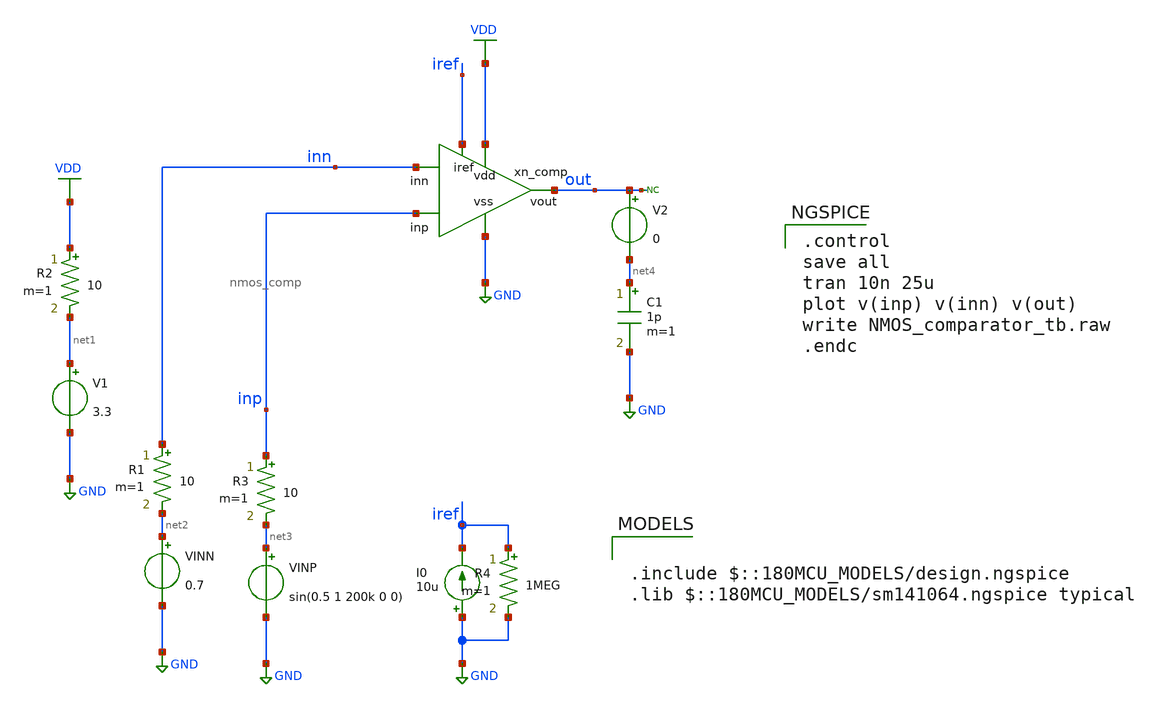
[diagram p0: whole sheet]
** sch_path: designs/libs/tb_analog/tb_nmos_comp/tb_nmos_comp.sch
**.subckt tb_nmos_comp
I0 GND iref 10u
V1 net1 GND 3.3
VINP net3 GND sin(0.5 1 200k 0 0)
* noconn out
VINN net2 GND 0.7
C1 net4 GND 1p m=1
R3 inp net3 10 m=1
R1 inn net2 10 m=1
R2 VDD net1 10 m=1
R4 iref GND 1MEG m=1
V2 out net4 0
xn_comp VDD out inp GND inn iref nmos_comp
**** begin user architecture code

.control
save all
tran 10n 25u
plot v(inp) v(inn) v(out)
write NMOS_comparator_tb.raw
.endc



.include $::180MCU_MODELS/design.ngspice
.lib $::180MCU_MODELS/sm141064.ngspice typical

**** end user architecture code
**.ends

* expanding   symbol:  pmos_comp/nmos_comp.sym # of pins=6
** sym_path: designs/libs/core_analog/nmos_comp/nmos_comp.sym
** sch_path: designs/libs/core_analog/nmos_comp/nmos_comp.sch
.subckt nmos_comp vdd vout inp vss inn iref
*.ipin vss
*.ipin vdd
*.ipin iref
*.ipin inn
*.ipin inp
*.opin vout
XM3 net1 net1 vss vss nfet_03v3 L=1u W=3.5u nf=1 ad='int((nf+1)/2) * W/nf * 0.18u' as='int((nf+2)/2) * W/nf * 0.18u'
+ pd='2*int((nf+1)/2) * (W/nf + 0.18u)' ps='2*int((nf+2)/2) * (W/nf + 0.18u)' nrd='0.18u / W' nrs='0.18u / W'
+ sa=0 sb=0 sd=0 m=1
XM4 vout net1 vss vss nfet_03v3 L=1u W=3.5u nf=1 ad='int((nf+1)/2) * W/nf * 0.18u' as='int((nf+2)/2) * W/nf * 0.18u'
+ pd='2*int((nf+1)/2) * (W/nf + 0.18u)' ps='2*int((nf+2)/2) * (W/nf + 0.18u)' nrd='0.18u / W' nrs='0.18u / W'
+ sa=0 sb=0 sd=0 m=1
XM1 net2 inn i_bias_n vss nfet_03v3 L=1u W=4u nf=1 ad='int((nf+1)/2) * W/nf * 0.18u' as='int((nf+2)/2) * W/nf * 0.18u'
+ pd='2*int((nf+1)/2) * (W/nf + 0.18u)' ps='2*int((nf+2)/2) * (W/nf + 0.18u)' nrd='0.18u / W' nrs='0.18u / W'
+ sa=0 sb=0 sd=0 m=1
XM2 net3 inp i_bias_n vss nfet_03v3 L=1u W=4u nf=1 ad='int((nf+1)/2) * W/nf * 0.18u' as='int((nf+2)/2) * W/nf * 0.18u'
+ pd='2*int((nf+1)/2) * (W/nf + 0.18u)' ps='2*int((nf+2)/2) * (W/nf + 0.18u)' nrd='0.18u / W' nrs='0.18u / W'
+ sa=0 sb=0 sd=0 m=1
XM10 net1 net2 vdd vdd pfet_03v3 L=0.5u W=16.5u nf=4 ad='int((nf+1)/2) * W/nf * 0.18u' as='int((nf+2)/2) * W/nf * 0.18u'
+ pd='2*int((nf+1)/2) * (W/nf + 0.18u)' ps='2*int((nf+2)/2) * (W/nf + 0.18u)' nrd='0.18u / W' nrs='0.18u / W'
+ sa=0 sb=0 sd=0 m=1
XM6 net3 net3 vdd vdd pfet_03v3 L=0.5u W=10u nf=2 ad='int((nf+1)/2) * W/nf * 0.18u' as='int((nf+2)/2) * W/nf * 0.18u'
+ pd='2*int((nf+1)/2) * (W/nf + 0.18u)' ps='2*int((nf+2)/2) * (W/nf + 0.18u)' nrd='0.18u / W' nrs='0.18u / W'
+ sa=0 sb=0 sd=0 m=1
XM5 net2 net2 vdd vdd pfet_03v3 L=0.5u W=10u nf=2 ad='int((nf+1)/2) * W/nf * 0.18u' as='int((nf+2)/2) * W/nf * 0.18u'
+ pd='2*int((nf+1)/2) * (W/nf + 0.18u)' ps='2*int((nf+2)/2) * (W/nf + 0.18u)' nrd='0.18u / W' nrs='0.18u / W'
+ sa=0 sb=0 sd=0 m=1
XM9 vout net3 vdd vdd pfet_03v3 L=0.5u W=16.5u nf=4 ad='int((nf+1)/2) * W/nf * 0.18u' as='int((nf+2)/2) * W/nf * 0.18u'
+ pd='2*int((nf+1)/2) * (W/nf + 0.18u)' ps='2*int((nf+2)/2) * (W/nf + 0.18u)' nrd='0.18u / W' nrs='0.18u / W'
+ sa=0 sb=0 sd=0 m=1
XM8 iref iref vss vss nfet_03v3 L=1u W=5u nf=1 ad='int((nf+1)/2) * W/nf * 0.18u' as='int((nf+2)/2) * W/nf * 0.18u'
+ pd='2*int((nf+1)/2) * (W/nf + 0.18u)' ps='2*int((nf+2)/2) * (W/nf + 0.18u)' nrd='0.18u / W' nrs='0.18u / W'
+ sa=0 sb=0 sd=0 m=1
XM7 i_bias_n iref vss vss nfet_03v3 L=1u W=10u nf=2 ad='int((nf+1)/2) * W/nf * 0.18u' as='int((nf+2)/2) * W/nf * 0.18u'
+ pd='2*int((nf+1)/2) * (W/nf + 0.18u)' ps='2*int((nf+2)/2) * (W/nf + 0.18u)' nrd='0.18u / W' nrs='0.18u / W'
+ sa=0 sb=0 sd=0 m=1
XM12 net2 net3 vdd vdd pfet_03v3 L=0.5u W=20u nf=4 ad='int((nf+1)/2) * W/nf * 0.18u' as='int((nf+2)/2) * W/nf * 0.18u'
+ pd='2*int((nf+1)/2) * (W/nf + 0.18u)' ps='2*int((nf+2)/2) * (W/nf + 0.18u)' nrd='0.18u / W' nrs='0.18u / W'
+ sa=0 sb=0 sd=0 m=1
XM13 net3 net2 vdd vdd pfet_03v3 L=0.5u W=20u nf=4 ad='int((nf+1)/2) * W/nf * 0.18u' as='int((nf+2)/2) * W/nf * 0.18u'
+ pd='2*int((nf+1)/2) * (W/nf + 0.18u)' ps='2*int((nf+2)/2) * (W/nf + 0.18u)' nrd='0.18u / W' nrs='0.18u / W'
+ sa=0 sb=0 sd=0 m=1
.ends

.GLOBAL GND
.GLOBAL VDD
.end
